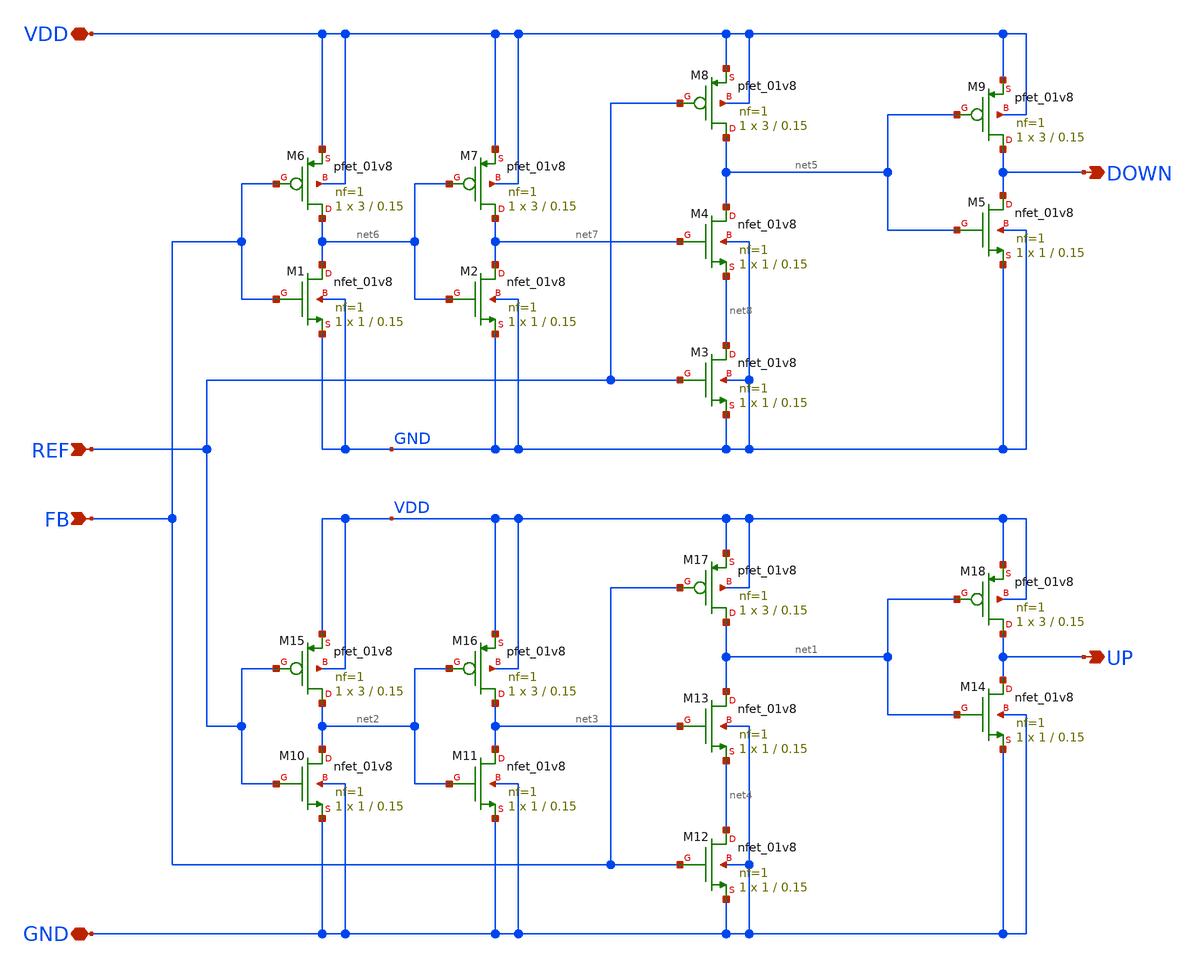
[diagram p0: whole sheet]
** sch_path: design/phasefrequencydetector/phasefrequencydetector.sch
**.subckt phasefrequencydetector FB DOWN VDD GND UP REF
*.ipin FB
*.opin DOWN
*.iopin VDD
*.iopin GND
*.opin UP
*.ipin REF
XM1 net6 FB GND GND sky130_fd_pr__nfet_01v8 L=0.15 W=1 nf=1 ad='W * 0.29' as='W * 0.29' pd='2 * (W + 0.29)'
+ ps='2 * (W + 0.29)' nrd='0.29 / W' nrs='0.29 / W' sa=0 sb=0 sd=0 mult=1 m=1
XM2 net7 net6 GND GND sky130_fd_pr__nfet_01v8 L=0.15 W=1 nf=1 ad='W * 0.29' as='W * 0.29' pd='2 * (W + 0.29)'
+ ps='2 * (W + 0.29)' nrd='0.29 / W' nrs='0.29 / W' sa=0 sb=0 sd=0 mult=1 m=1
XM3 net8 REF GND GND sky130_fd_pr__nfet_01v8 L=0.15 W=1 nf=1 ad='W * 0.29' as='W * 0.29' pd='2 * (W + 0.29)'
+ ps='2 * (W + 0.29)' nrd='0.29 / W' nrs='0.29 / W' sa=0 sb=0 sd=0 mult=1 m=1
XM4 net5 net7 net8 GND sky130_fd_pr__nfet_01v8 L=0.15 W=1 nf=1 ad='W * 0.29' as='W * 0.29' pd='2 * (W + 0.29)'
+ ps='2 * (W + 0.29)' nrd='0.29 / W' nrs='0.29 / W' sa=0 sb=0 sd=0 mult=1 m=1
XM5 DOWN net5 GND GND sky130_fd_pr__nfet_01v8 L=0.15 W=1 nf=1 ad='W * 0.29' as='W * 0.29' pd='2 * (W + 0.29)'
+ ps='2 * (W + 0.29)' nrd='0.29 / W' nrs='0.29 / W' sa=0 sb=0 sd=0 mult=1 m=1
XM6 net6 FB VDD VDD sky130_fd_pr__pfet_01v8 L=0.15 W=3 nf=1 ad='W * 0.29' as='W * 0.29' pd='2 * (W + 0.29)'
+ ps='2 * (W + 0.29)' nrd='0.29 / W' nrs='0.29 / W' sa=0 sb=0 sd=0 mult=1 m=1
XM7 net7 net6 VDD VDD sky130_fd_pr__pfet_01v8 L=0.15 W=3 nf=1 ad='W * 0.29' as='W * 0.29' pd='2 * (W + 0.29)'
+ ps='2 * (W + 0.29)' nrd='0.29 / W' nrs='0.29 / W' sa=0 sb=0 sd=0 mult=1 m=1
XM8 net5 REF VDD VDD sky130_fd_pr__pfet_01v8 L=0.15 W=3 nf=1 ad='W * 0.29' as='W * 0.29' pd='2 * (W + 0.29)'
+ ps='2 * (W + 0.29)' nrd='0.29 / W' nrs='0.29 / W' sa=0 sb=0 sd=0 mult=1 m=1
XM9 DOWN net5 VDD VDD sky130_fd_pr__pfet_01v8 L=0.15 W=3 nf=1 ad='W * 0.29' as='W * 0.29' pd='2 * (W + 0.29)'
+ ps='2 * (W + 0.29)' nrd='0.29 / W' nrs='0.29 / W' sa=0 sb=0 sd=0 mult=1 m=1
XM10 net2 REF GND GND sky130_fd_pr__nfet_01v8 L=0.15 W=1 nf=1 ad='W * 0.29' as='W * 0.29' pd='2 * (W + 0.29)'
+ ps='2 * (W + 0.29)' nrd='0.29 / W' nrs='0.29 / W' sa=0 sb=0 sd=0 mult=1 m=1
XM11 net3 net2 GND GND sky130_fd_pr__nfet_01v8 L=0.15 W=1 nf=1 ad='W * 0.29' as='W * 0.29' pd='2 * (W + 0.29)'
+ ps='2 * (W + 0.29)' nrd='0.29 / W' nrs='0.29 / W' sa=0 sb=0 sd=0 mult=1 m=1
XM12 net4 FB GND GND sky130_fd_pr__nfet_01v8 L=0.15 W=1 nf=1 ad='W * 0.29' as='W * 0.29' pd='2 * (W + 0.29)'
+ ps='2 * (W + 0.29)' nrd='0.29 / W' nrs='0.29 / W' sa=0 sb=0 sd=0 mult=1 m=1
XM13 net1 net3 net4 GND sky130_fd_pr__nfet_01v8 L=0.15 W=1 nf=1 ad='W * 0.29' as='W * 0.29' pd='2 * (W + 0.29)'
+ ps='2 * (W + 0.29)' nrd='0.29 / W' nrs='0.29 / W' sa=0 sb=0 sd=0 mult=1 m=1
XM14 UP net1 GND GND sky130_fd_pr__nfet_01v8 L=0.15 W=1 nf=1 ad='W * 0.29' as='W * 0.29' pd='2 * (W + 0.29)'
+ ps='2 * (W + 0.29)' nrd='0.29 / W' nrs='0.29 / W' sa=0 sb=0 sd=0 mult=1 m=1
XM15 net2 REF VDD VDD sky130_fd_pr__pfet_01v8 L=0.15 W=3 nf=1 ad='W * 0.29' as='W * 0.29' pd='2 * (W + 0.29)'
+ ps='2 * (W + 0.29)' nrd='0.29 / W' nrs='0.29 / W' sa=0 sb=0 sd=0 mult=1 m=1
XM16 net3 net2 VDD VDD sky130_fd_pr__pfet_01v8 L=0.15 W=3 nf=1 ad='W * 0.29' as='W * 0.29' pd='2 * (W + 0.29)'
+ ps='2 * (W + 0.29)' nrd='0.29 / W' nrs='0.29 / W' sa=0 sb=0 sd=0 mult=1 m=1
XM17 net1 FB VDD VDD sky130_fd_pr__pfet_01v8 L=0.15 W=3 nf=1 ad='W * 0.29' as='W * 0.29' pd='2 * (W + 0.29)'
+ ps='2 * (W + 0.29)' nrd='0.29 / W' nrs='0.29 / W' sa=0 sb=0 sd=0 mult=1 m=1
XM18 UP net1 VDD VDD sky130_fd_pr__pfet_01v8 L=0.15 W=3 nf=1 ad='W * 0.29' as='W * 0.29' pd='2 * (W + 0.29)'
+ ps='2 * (W + 0.29)' nrd='0.29 / W' nrs='0.29 / W' sa=0 sb=0 sd=0 mult=1 m=1
**.ends
.end
